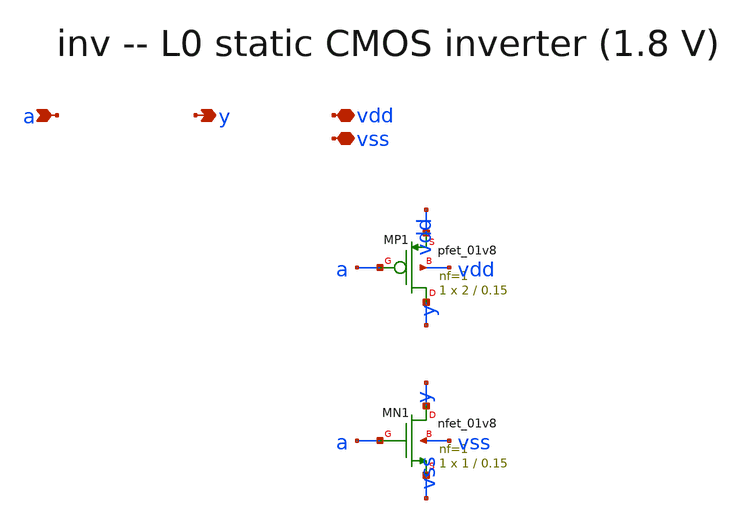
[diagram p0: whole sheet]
** sch_path: xschem/onetops/inv.sch
**.subckt inv a y vdd vss
*.ipin a
*.opin y
*.iopin vdd
*.iopin vss
XMP1 y a vdd vdd sky130_fd_pr__pfet_01v8 L=0.15 W=2 nf=1 ad='int((1 + 1)/2) * 2 / 1 * 0.29' as='int((1 + 2)/2) * 2 / 1 * 0.29'
+ pd='2*int((1 + 1)/2) * (2 / 1 + 0.29)' ps='2*int((1 + 2)/2) * (2 / 1 + 0.29)' nrd='0.29 / 2 ' nrs='0.29 / 2 '
+ sa=0 sb=0 sd=0 mult=1 m=1
XMN1 y a vss vss sky130_fd_pr__nfet_01v8 L=0.15 W=1 nf=1 ad='int((1 + 1)/2) * 1 / 1 * 0.29' as='int((1 + 2)/2) * 1 / 1 * 0.29'
+ pd='2*int((1 + 1)/2) * (1 / 1 + 0.29)' ps='2*int((1 + 2)/2) * (1 / 1 + 0.29)' nrd='0.29 / 1 ' nrs='0.29 / 1 '
+ sa=0 sb=0 sd=0 mult=1 m=1
**.ends
.end
